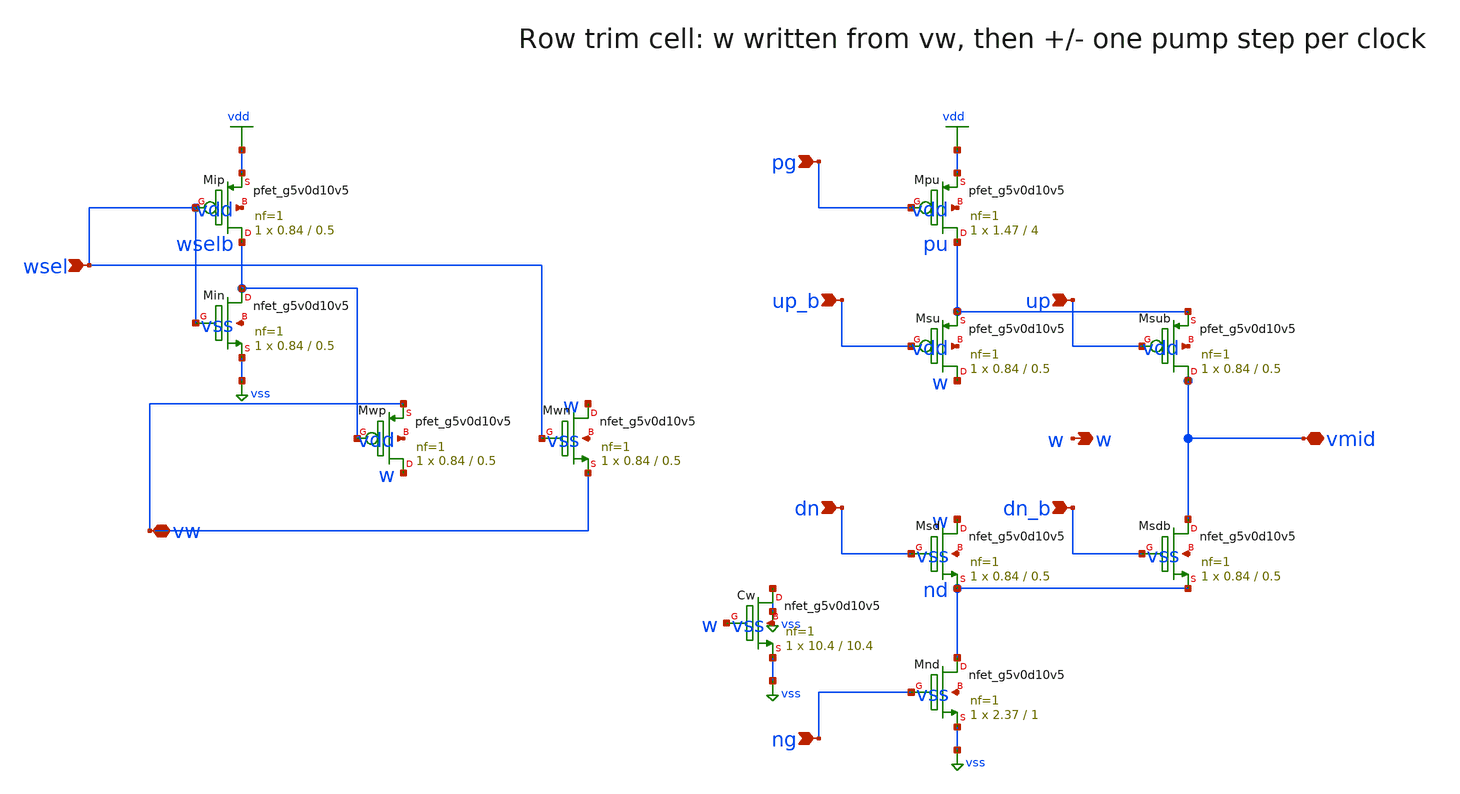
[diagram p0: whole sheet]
** sch_path: xschem/rt5w_trimcell.sch
**.subckt rt5w_trimcell vw wsel pg ng up_b up dn dn_b vmid w
*.iopin vw
*.ipin wsel
*.ipin pg
*.ipin ng
*.ipin up_b
*.ipin up
*.ipin dn
*.ipin dn_b
*.iopin vmid
*.opin w
XMpu pu pg vdd vdd sky130_fd_pr__pfet_g5v0d10v5 L=4 W=1.47 nf=1 ad=0.4263 as=0.4263 pd=3.52 ps=3.52
+ nrd=0.1973 nrs=0.1973 sa=0 sb=0 sd=0 mult=1 m=1
XMsu w up_b pu vdd sky130_fd_pr__pfet_g5v0d10v5 L=0.5 W=0.84 nf=1 ad=0.2436 as=0.2436 pd=2.26
+ ps=2.26 nrd=0.3452 nrs=0.3452 sa=0 sb=0 sd=0 mult=1 m=1
XMsub vmid up pu vdd sky130_fd_pr__pfet_g5v0d10v5 L=0.5 W=0.84 nf=1 ad=0.2436 as=0.2436 pd=2.26
+ ps=2.26 nrd=0.3452 nrs=0.3452 sa=0 sb=0 sd=0 mult=1 m=1
XMsd w dn nd vss sky130_fd_pr__nfet_g5v0d10v5 L=0.5 W=0.84 nf=1 ad=0.2436 as=0.2436 pd=2.26 ps=2.26
+ nrd=0.3452 nrs=0.3452 sa=0 sb=0 sd=0 mult=1 m=1
XMsdb vmid dn_b nd vss sky130_fd_pr__nfet_g5v0d10v5 L=0.5 W=0.84 nf=1 ad=0.2436 as=0.2436 pd=2.26
+ ps=2.26 nrd=0.3452 nrs=0.3452 sa=0 sb=0 sd=0 mult=1 m=1
XMnd nd ng vss vss sky130_fd_pr__nfet_g5v0d10v5 L=1 W=2.37 nf=1 ad=0.6873 as=0.6873 pd=5.32 ps=5.32
+ nrd=0.1224 nrs=0.1224 sa=0 sb=0 sd=0 mult=1 m=1
XCw vss w vss vss sky130_fd_pr__nfet_g5v0d10v5 L=10.4 W=10.4 nf=1 ad=3.016 as=3.016 pd=21.38
+ ps=21.38 nrd=0.02788 nrs=0.02788 sa=0 sb=0 sd=0 mult=1 m=1
XMwn w wsel vw vss sky130_fd_pr__nfet_g5v0d10v5 L=0.5 W=0.84 nf=1 ad=0.2436 as=0.2436 pd=2.26
+ ps=2.26 nrd=0.3452 nrs=0.3452 sa=0 sb=0 sd=0 mult=1 m=1
XMwp w wselb vw vdd sky130_fd_pr__pfet_g5v0d10v5 L=0.5 W=0.84 nf=1 ad=0.2436 as=0.2436 pd=2.26
+ ps=2.26 nrd=0.3452 nrs=0.3452 sa=0 sb=0 sd=0 mult=1 m=1
XMip wselb wsel vdd vdd sky130_fd_pr__pfet_g5v0d10v5 L=0.5 W=0.84 nf=1 ad=0.2436 as=0.2436 pd=2.26
+ ps=2.26 nrd=0.3452 nrs=0.3452 sa=0 sb=0 sd=0 mult=1 m=1
XMin wselb wsel vss vss sky130_fd_pr__nfet_g5v0d10v5 L=0.5 W=0.84 nf=1 ad=0.2436 as=0.2436 pd=2.26
+ ps=2.26 nrd=0.3452 nrs=0.3452 sa=0 sb=0 sd=0 mult=1 m=1
**.ends
.GLOBAL vdd
.GLOBAL vss
.end
